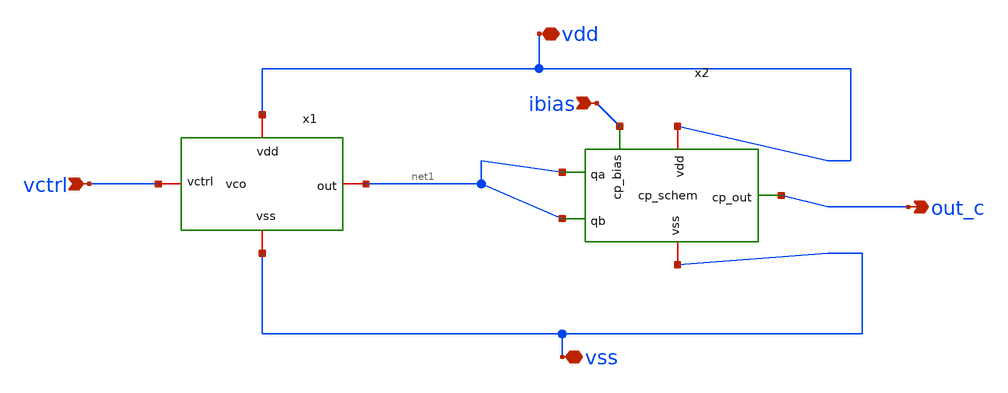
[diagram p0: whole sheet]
** sch_path: xschem/top_vco_divider.sch
**.subckt top_vco_divider vctrl out_c vdd vss ibias
*.ipin vctrl
*.opin out_c
*.iopin vdd
*.iopin vss
*.ipin ibias
x1 vdd net1 vctrl vss vco
x2 vdd ibias net1 out_c net1 vss cp_schem
**.ends

* expanding   symbol:  PLL_FOLDER/vco/vco.sym # of pins=4
** sym_path: PLL_FOLDER/vco/vco.sym
** sch_path: PLL_FOLDER/vco/vco.sch
.subckt vco vdd out vctrl vss
*.iopin vdd
*.iopin vss
*.iopin out
*.iopin vctrl
XM1 net1 vctrl vss vss sky130_fd_pr__nfet_01v8 L=0.15 W=30 nf=5 ad='int((nf+1)/2) * W/nf * 0.29' as='int((nf+2)/2) * W/nf * 0.29'
+ pd='2*int((nf+1)/2) * (W/nf + 0.29)' ps='2*int((nf+2)/2) * (W/nf + 0.29)' nrd='0.29 / W' nrs='0.29 / W'
+ sa=0 sb=0 sd=0 mult=1 m=1
XM2 net1 net1 vdd vdd sky130_fd_pr__pfet_01v8 L=0.15 W=90 nf=5 ad='int((nf+1)/2) * W/nf * 0.29' as='int((nf+2)/2) * W/nf * 0.29'
+ pd='2*int((nf+1)/2) * (W/nf + 0.29)' ps='2*int((nf+2)/2) * (W/nf + 0.29)' nrd='0.29 / W' nrs='0.29 / W'
+ sa=0 sb=0 sd=0 mult=1 m=1
XM3 net4 net1 vdd vdd sky130_fd_pr__pfet_01v8 L=0.15 W=80 nf=10 ad='int((nf+1)/2) * W/nf * 0.29' as='int((nf+2)/2) * W/nf * 0.29'
+ pd='2*int((nf+1)/2) * (W/nf + 0.29)' ps='2*int((nf+2)/2) * (W/nf + 0.29)' nrd='0.29 / W' nrs='0.29 / W'
+ sa=0 sb=0 sd=0 mult=1 m=1
XM4 net3 out net4 net4 sky130_fd_pr__pfet_01v8 L=0.15 W=80 nf=10 ad='int((nf+1)/2) * W/nf * 0.29' as='int((nf+2)/2) * W/nf * 0.29'
+ pd='2*int((nf+1)/2) * (W/nf + 0.29)' ps='2*int((nf+2)/2) * (W/nf + 0.29)' nrd='0.29 / W' nrs='0.29 / W'
+ sa=0 sb=0 sd=0 mult=1 m=1
XM5 net2 vctrl vss vss sky130_fd_pr__nfet_01v8 L=0.15 W=30 nf=10 ad='int((nf+1)/2) * W/nf * 0.29' as='int((nf+2)/2) * W/nf * 0.29'
+ pd='2*int((nf+1)/2) * (W/nf + 0.29)' ps='2*int((nf+2)/2) * (W/nf + 0.29)' nrd='0.29 / W' nrs='0.29 / W'
+ sa=0 sb=0 sd=0 mult=1 m=1
XM6 net3 out net2 vss sky130_fd_pr__nfet_01v8 L=0.15 W=30 nf=10 ad='int((nf+1)/2) * W/nf * 0.29' as='int((nf+2)/2) * W/nf * 0.29'
+ pd='2*int((nf+1)/2) * (W/nf + 0.29)' ps='2*int((nf+2)/2) * (W/nf + 0.29)' nrd='0.29 / W' nrs='0.29 / W'
+ sa=0 sb=0 sd=0 mult=1 m=1
XM7 net7 net1 vdd vdd sky130_fd_pr__pfet_01v8 L=0.15 W=160 nf=20 ad='int((nf+1)/2) * W/nf * 0.29' as='int((nf+2)/2) * W/nf * 0.29'
+ pd='2*int((nf+1)/2) * (W/nf + 0.29)' ps='2*int((nf+2)/2) * (W/nf + 0.29)' nrd='0.29 / W' nrs='0.29 / W'
+ sa=0 sb=0 sd=0 mult=1 m=1
XM8 net6 net3 net7 net7 sky130_fd_pr__pfet_01v8 L=0.15 W=160 nf=20 ad='int((nf+1)/2) * W/nf * 0.29' as='int((nf+2)/2) * W/nf * 0.29'
+ pd='2*int((nf+1)/2) * (W/nf + 0.29)' ps='2*int((nf+2)/2) * (W/nf + 0.29)' nrd='0.29 / W' nrs='0.29 / W'
+ sa=0 sb=0 sd=0 mult=1 m=1
XM9 net5 vctrl vss vss sky130_fd_pr__nfet_01v8 L=0.15 W=60 nf=20 ad='int((nf+1)/2) * W/nf * 0.29' as='int((nf+2)/2) * W/nf * 0.29'
+ pd='2*int((nf+1)/2) * (W/nf + 0.29)' ps='2*int((nf+2)/2) * (W/nf + 0.29)' nrd='0.29 / W' nrs='0.29 / W'
+ sa=0 sb=0 sd=0 mult=1 m=1
XM10 net6 net3 net5 vss sky130_fd_pr__nfet_01v8 L=0.15 W=60 nf=20 ad='int((nf+1)/2) * W/nf * 0.29' as='int((nf+2)/2) * W/nf * 0.29'
+ pd='2*int((nf+1)/2) * (W/nf + 0.29)' ps='2*int((nf+2)/2) * (W/nf + 0.29)' nrd='0.29 / W' nrs='0.29 / W'
+ sa=0 sb=0 sd=0 mult=1 m=1
XM11 net9 net1 vdd vdd sky130_fd_pr__pfet_01v8 L=0.15 W=240 nf=30 ad='int((nf+1)/2) * W/nf * 0.29' as='int((nf+2)/2) * W/nf * 0.29'
+ pd='2*int((nf+1)/2) * (W/nf + 0.29)' ps='2*int((nf+2)/2) * (W/nf + 0.29)' nrd='0.29 / W' nrs='0.29 / W'
+ sa=0 sb=0 sd=0 mult=1 m=1
XM12 out net6 net9 net9 sky130_fd_pr__pfet_01v8 L=0.15 W=240 nf=30 ad='int((nf+1)/2) * W/nf * 0.29' as='int((nf+2)/2) * W/nf * 0.29'
+ pd='2*int((nf+1)/2) * (W/nf + 0.29)' ps='2*int((nf+2)/2) * (W/nf + 0.29)' nrd='0.29 / W' nrs='0.29 / W'
+ sa=0 sb=0 sd=0 mult=1 m=1
XM13 net8 vctrl vss vss sky130_fd_pr__nfet_01v8 L=0.15 W=90 nf=30 ad='int((nf+1)/2) * W/nf * 0.29' as='int((nf+2)/2) * W/nf * 0.29'
+ pd='2*int((nf+1)/2) * (W/nf + 0.29)' ps='2*int((nf+2)/2) * (W/nf + 0.29)' nrd='0.29 / W' nrs='0.29 / W'
+ sa=0 sb=0 sd=0 mult=1 m=1
XM14 out net6 net8 vss sky130_fd_pr__nfet_01v8 L=0.15 W=90 nf=30 ad='int((nf+1)/2) * W/nf * 0.29' as='int((nf+2)/2) * W/nf * 0.29'
+ pd='2*int((nf+1)/2) * (W/nf + 0.29)' ps='2*int((nf+2)/2) * (W/nf + 0.29)' nrd='0.29 / W' nrs='0.29 / W'
+ sa=0 sb=0 sd=0 mult=1 m=1
.ends


* expanding   symbol:  PLL_FOLDER/cp/cp_schem.sym # of pins=6
** sym_path: xschem/PLL_FOLDER/cp/cp_schem.sym
** sch_path: xschem/PLL_FOLDER/cp/cp_schem.sch
.subckt cp_schem vdd cp_bias qa cp_out qb vss
*.ipin qa
*.ipin qb
*.opin cp_out
*.iopin vdd
*.iopin vss
*.ipin cp_bias
XM1 n1 n1 vdd vdd sky130_fd_pr__pfet_01v8 L=0.3 W=6 nf=3 ad='int((nf+1)/2) * W/nf * 0.29' as='int((nf+2)/2) * W/nf * 0.29'
+ pd='2*int((nf+1)/2) * (W/nf + 0.29)' ps='2*int((nf+2)/2) * (W/nf + 0.29)' nrd='0.29 / W' nrs='0.29 / W'
+ sa=0 sb=0 sd=0 mult=1 m=1
XM2 n1 bias vss vss sky130_fd_pr__nfet_01v8 L=0.3 W=2 nf=2 ad='int((nf+1)/2) * W/nf * 0.29' as='int((nf+2)/2) * W/nf * 0.29'
+ pd='2*int((nf+1)/2) * (W/nf + 0.29)' ps='2*int((nf+2)/2) * (W/nf + 0.29)' nrd='0.29 / W' nrs='0.29 / W'
+ sa=0 sb=0 sd=0 mult=1 m=1
XM3 bias bias vss vss sky130_fd_pr__nfet_01v8 L=0.30 W=2 nf=2 ad='int((nf+1)/2) * W/nf * 0.29' as='int((nf+2)/2) * W/nf * 0.29'
+ pd='2*int((nf+1)/2) * (W/nf + 0.29)' ps='2*int((nf+2)/2) * (W/nf + 0.29)' nrd='0.29 / W' nrs='0.29 / W'
+ sa=0 sb=0 sd=0 mult=1 m=1
XM4 n2 n1 vdd vdd sky130_fd_pr__pfet_01v8 L=0.3 W=14 nf=7 ad='int((nf+1)/2) * W/nf * 0.29' as='int((nf+2)/2) * W/nf * 0.29'
+ pd='2*int((nf+1)/2) * (W/nf + 0.29)' ps='2*int((nf+2)/2) * (W/nf + 0.29)' nrd='0.29 / W' nrs='0.29 / W'
+ sa=0 sb=0 sd=0 mult=1 m=1
XM5 n3 bias vss vss sky130_fd_pr__nfet_01v8 L=0.3 W=0.7 nf=1 ad='int((nf+1)/2) * W/nf * 0.29' as='int((nf+2)/2) * W/nf * 0.29'
+ pd='2*int((nf+1)/2) * (W/nf + 0.29)' ps='2*int((nf+2)/2) * (W/nf + 0.29)' nrd='0.29 / W' nrs='0.29 / W'
+ sa=0 sb=0 sd=0 mult=1 m=1
XM6 cp_out qa n2 vdd sky130_fd_pr__pfet_01v8 L=2 W=1 nf=1 ad='int((nf+1)/2) * W/nf * 0.29' as='int((nf+2)/2) * W/nf * 0.29'
+ pd='2*int((nf+1)/2) * (W/nf + 0.29)' ps='2*int((nf+2)/2) * (W/nf + 0.29)' nrd='0.29 / W' nrs='0.29 / W'
+ sa=0 sb=0 sd=0 mult=1 m=1
XM7 cp_out qb n3 vss sky130_fd_pr__nfet_01v8 L=5 W=1 nf=1 ad='int((nf+1)/2) * W/nf * 0.29' as='int((nf+2)/2) * W/nf * 0.29'
+ pd='2*int((nf+1)/2) * (W/nf + 0.29)' ps='2*int((nf+2)/2) * (W/nf + 0.29)' nrd='0.29 / W' nrs='0.29 / W'
+ sa=0 sb=0 sd=0 mult=1 m=1
XM8 bias cp_bias vdd vdd sky130_fd_pr__pfet_01v8 L=0.3 W=18 nf=9 ad='int((nf+1)/2) * W/nf * 0.29' as='int((nf+2)/2) * W/nf * 0.29'
+ pd='2*int((nf+1)/2) * (W/nf + 0.29)' ps='2*int((nf+2)/2) * (W/nf + 0.29)' nrd='0.29 / W' nrs='0.29 / W'
+ sa=0 sb=0 sd=0 mult=1 m=1
.ends

.end
